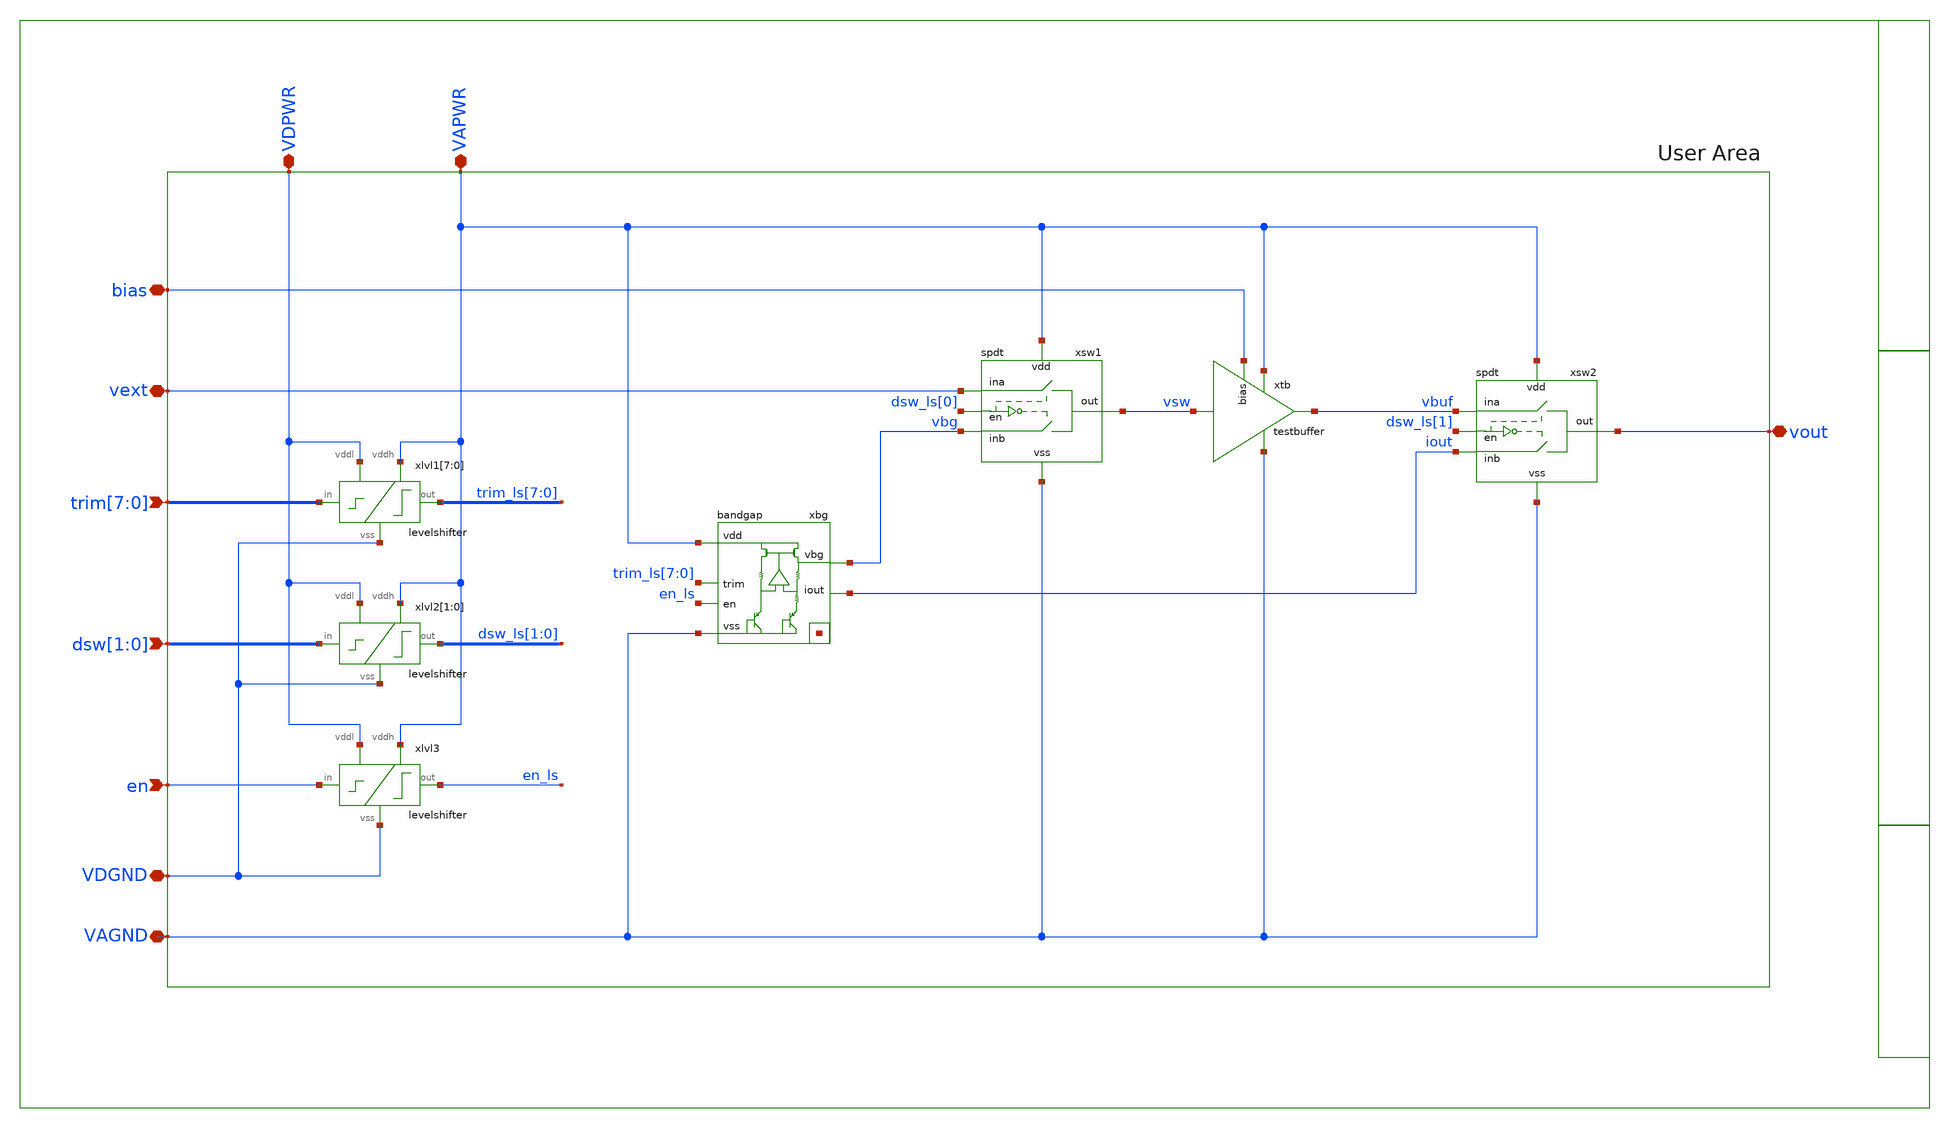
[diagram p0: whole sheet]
** sch_path: xschem/sch/top/gf180mcu_cw_ip_vref.sch
**.subckt gf180mcu_cw_ip_vref VDGND VDPWR VAPWR bias
*+ trim[7],trim[6],trim[5],trim[4],trim[3],trim[2],trim[1],trim[0] dsw[1],dsw[0] vout vext en VAGND
*.iopin VDGND
*.iopin VDPWR
*.iopin VAPWR
*.iopin bias
*.ipin trim[7],trim[6],trim[5],trim[4],trim[3],trim[2],trim[1],trim[0]
*.ipin dsw[1],dsw[0]
*.iopin vout
*.iopin vext
*.ipin en
*.iopin VAGND
xtb VAPWR vbuf vsw VAGND bias testbuffer
xsw1 vsw dsw_ls[0] VAPWR vbg VAGND vext spdt
xsw2 vout dsw_ls[1] VAPWR iout VAGND vbuf spdt
xlvl1[7] VDPWR trim[7] trim_ls[7] VDGND VAPWR levelshifter
xlvl1[6] VDPWR trim[6] trim_ls[6] VDGND VAPWR levelshifter
xlvl1[5] VDPWR trim[5] trim_ls[5] VDGND VAPWR levelshifter
xlvl1[4] VDPWR trim[4] trim_ls[4] VDGND VAPWR levelshifter
xlvl1[3] VDPWR trim[3] trim_ls[3] VDGND VAPWR levelshifter
xlvl1[2] VDPWR trim[2] trim_ls[2] VDGND VAPWR levelshifter
xlvl1[1] VDPWR trim[1] trim_ls[1] VDGND VAPWR levelshifter
xlvl1[0] VDPWR trim[0] trim_ls[0] VDGND VAPWR levelshifter
xlvl2[1] VDPWR dsw[1] dsw_ls[1] VDGND VAPWR levelshifter
xlvl2[0] VDPWR dsw[0] dsw_ls[0] VDGND VAPWR levelshifter
xbg VAPWR vbg VAGND net1[7] net1[6] net1[5] net1[4] net1[3] net1[2] net1[1] net1[0] trim_ls[7]
+ trim_ls[6] trim_ls[5] trim_ls[4] trim_ls[3] trim_ls[2] trim_ls[1] trim_ls[0] iout en_ls bandgap
xlvl3 VDPWR en en_ls VDGND VAPWR levelshifter
**.ends
.end
